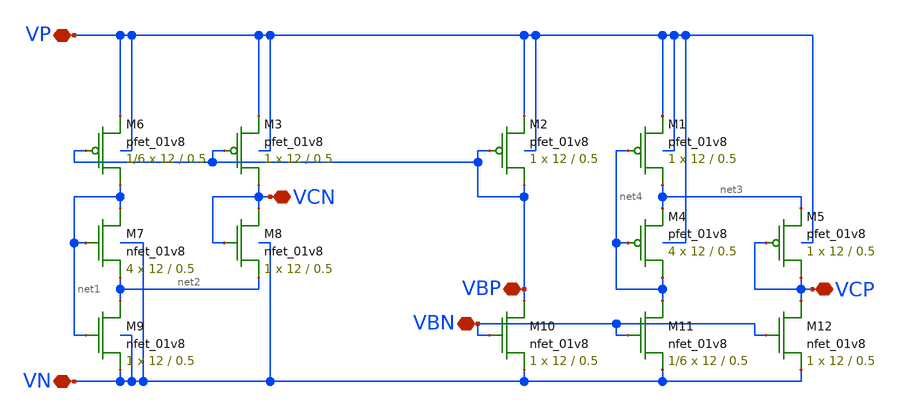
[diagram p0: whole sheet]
** sch_path: mp3/schematics/bias_generator (3rd copy).sch
**.subckt bias_generator (3rd copy) VP VN VBP VCN VCP VBN
*.iopin VP
*.iopin VN
*.iopin VBP
*.iopin VCN
*.iopin VCP
*.iopin VBN
XM4 net4 net4 net3 VDD sky130_fd_pr__pfet_01v8 L=0.5 W=12 nf=1 ad='int((nf+1)/2) * W/nf * 0.29' as='int((nf+2)/2) * W/nf * 0.29'
+ pd='2*int((nf+1)/2) * (W/nf + 0.29)' ps='2*int((nf+2)/2) * (W/nf + 0.29)' nrd='0.29 / W' nrs='0.29 / W'
+ sa=0 sb=0 sd=0 mult=4 m=4
XM5 VCP VCP net3 VDD sky130_fd_pr__pfet_01v8 L=0.5 W=12 nf=1 ad='int((nf+1)/2) * W/nf * 0.29' as='int((nf+2)/2) * W/nf * 0.29'
+ pd='2*int((nf+1)/2) * (W/nf + 0.29)' ps='2*int((nf+2)/2) * (W/nf + 0.29)' nrd='0.29 / W' nrs='0.29 / W'
+ sa=0 sb=0 sd=0 mult=1 m=1
XM1 net3 net4 VP VDD sky130_fd_pr__pfet_01v8 L=0.5 W=12 nf=1 ad='int((nf+1)/2) * W/nf * 0.29' as='int((nf+2)/2) * W/nf * 0.29'
+ pd='2*int((nf+1)/2) * (W/nf + 0.29)' ps='2*int((nf+2)/2) * (W/nf + 0.29)' nrd='0.29 / W' nrs='0.29 / W'
+ sa=0 sb=0 sd=0 mult=1 m=1
XM2 VBP VBP VP VDD sky130_fd_pr__pfet_01v8 L=0.5 W=12 nf=1 ad='int((nf+1)/2) * W/nf * 0.29' as='int((nf+2)/2) * W/nf * 0.29'
+ pd='2*int((nf+1)/2) * (W/nf + 0.29)' ps='2*int((nf+2)/2) * (W/nf + 0.29)' nrd='0.29 / W' nrs='0.29 / W'
+ sa=0 sb=0 sd=0 mult=1 m=1
XM3 VCN VBP VP VDD sky130_fd_pr__pfet_01v8 L=0.5 W=12 nf=1 ad='int((nf+1)/2) * W/nf * 0.29' as='int((nf+2)/2) * W/nf * 0.29'
+ pd='2*int((nf+1)/2) * (W/nf + 0.29)' ps='2*int((nf+2)/2) * (W/nf + 0.29)' nrd='0.29 / W' nrs='0.29 / W'
+ sa=0 sb=0 sd=0 mult=1 m=1
XM6 net1 VBP VP VDD sky130_fd_pr__pfet_01v8 L=0.5 W=12 nf=1 ad='int((nf+1)/2) * W/nf * 0.29' as='int((nf+2)/2) * W/nf * 0.29'
+ pd='2*int((nf+1)/2) * (W/nf + 0.29)' ps='2*int((nf+2)/2) * (W/nf + 0.29)' nrd='0.29 / W' nrs='0.29 / W'
+ sa=0 sb=0 sd=0 mult=1/6 m=1/6
XM10 VBP VBN VN GND sky130_fd_pr__nfet_01v8 L=0.5 W=12 nf=1 ad='int((nf+1)/2) * W/nf * 0.29' as='int((nf+2)/2) * W/nf * 0.29'
+ pd='2*int((nf+1)/2) * (W/nf + 0.29)' ps='2*int((nf+2)/2) * (W/nf + 0.29)' nrd='0.29 / W' nrs='0.29 / W'
+ sa=0 sb=0 sd=0 mult=1 m=1
XM11 net4 VBN VN GND sky130_fd_pr__nfet_01v8 L=0.5 W=12 nf=1 ad='int((nf+1)/2) * W/nf * 0.29' as='int((nf+2)/2) * W/nf * 0.29'
+ pd='2*int((nf+1)/2) * (W/nf + 0.29)' ps='2*int((nf+2)/2) * (W/nf + 0.29)' nrd='0.29 / W' nrs='0.29 / W'
+ sa=0 sb=0 sd=0 mult=1/6 m=1/6
XM12 VCP VBN VN GND sky130_fd_pr__nfet_01v8 L=0.5 W=12 nf=1 ad='int((nf+1)/2) * W/nf * 0.29' as='int((nf+2)/2) * W/nf * 0.29'
+ pd='2*int((nf+1)/2) * (W/nf + 0.29)' ps='2*int((nf+2)/2) * (W/nf + 0.29)' nrd='0.29 / W' nrs='0.29 / W'
+ sa=0 sb=0 sd=0 mult=1 m=1
XM9 net2 net1 VN GND sky130_fd_pr__nfet_01v8 L=0.5 W=12 nf=1 ad='int((nf+1)/2) * W/nf * 0.29' as='int((nf+2)/2) * W/nf * 0.29'
+ pd='2*int((nf+1)/2) * (W/nf + 0.29)' ps='2*int((nf+2)/2) * (W/nf + 0.29)' nrd='0.29 / W' nrs='0.29 / W'
+ sa=0 sb=0 sd=0 mult=1 m=1
XM8 VCN VCN net2 GND sky130_fd_pr__nfet_01v8 L=0.5 W=12 nf=1 ad='int((nf+1)/2) * W/nf * 0.29' as='int((nf+2)/2) * W/nf * 0.29'
+ pd='2*int((nf+1)/2) * (W/nf + 0.29)' ps='2*int((nf+2)/2) * (W/nf + 0.29)' nrd='0.29 / W' nrs='0.29 / W'
+ sa=0 sb=0 sd=0 mult=1 m=1
XM7 net1 net1 net2 GND sky130_fd_pr__nfet_01v8 L=0.5 W=12 nf=1 ad='int((nf+1)/2) * W/nf * 0.29' as='int((nf+2)/2) * W/nf * 0.29'
+ pd='2*int((nf+1)/2) * (W/nf + 0.29)' ps='2*int((nf+2)/2) * (W/nf + 0.29)' nrd='0.29 / W' nrs='0.29 / W'
+ sa=0 sb=0 sd=0 mult=4 m=4
**.ends
.end
